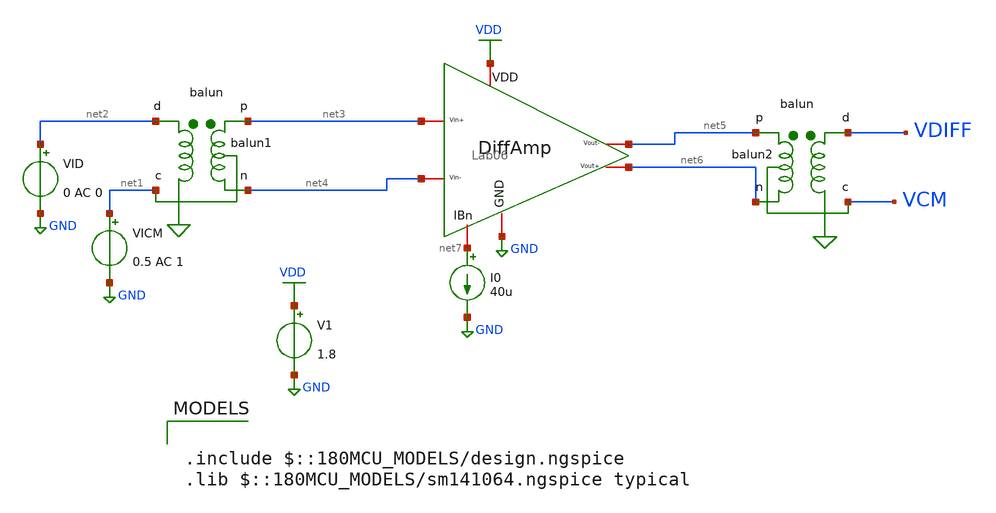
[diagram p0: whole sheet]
** sch_path: ITI_Labs/Lab6/Design/Lab06_Diff_Amp.sch
**.subckt Lab06_Diff_Amp
X1 VDD net7 net3 net4 net5 net6 GND Lab06
Xbalun1 net2 net1 net3 net4 balun
Xbalun2 VDIFF VCM net5 net6 balun
V1 VDD GND 1.8
I0 net7 GND 40u
VICM net1 GND 0.5 AC 1
VID net2 GND 0 AC 0
**** begin user architecture code


.include sim_script.sim



.include $::180MCU_MODELS/design.ngspice
.lib $::180MCU_MODELS/sm141064.ngspice typical

**** end user architecture code
**.ends
.GLOBAL VDD
.GLOBAL GND
.end
